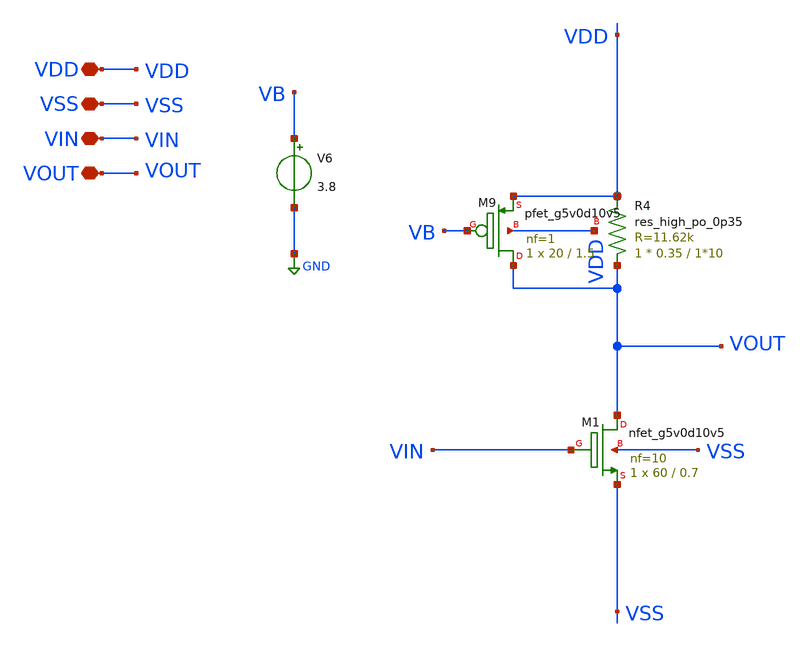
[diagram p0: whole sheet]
** sch_path: old stuff/amplifiers/single_stage_amps/stange_stages/cs_2/cs_2_stage.sch
**.subckt cs_2_stage VDD VSS VIN VOUT
*.iopin VDD
*.iopin VSS
*.iopin VIN
*.iopin VOUT
XM1 VOUT VIN VSS VSS sky130_fd_pr__nfet_g5v0d10v5 L=0.7 W=60 nf=10 ad='int((nf+1)/2) * W/nf * 0.29' as='int((nf+2)/2) * W/nf * 0.29'
+ pd='2*int((nf+1)/2) * (W/nf + 0.29)' ps='2*int((nf+2)/2) * (W/nf + 0.29)' nrd='0.29 / W' nrs='0.29 / W'
+ sa=0 sb=0 sd=0 mult=1 m=1
XR4 VOUT VDD VDD sky130_fd_pr__res_high_po_0p35 L=1*10 mult=1 m=1
XM9 VOUT VB VDD VDD sky130_fd_pr__pfet_g5v0d10v5 L=1.5 W=20 nf=1 ad='int((1 + 1)/2) * 20 / 1 * 0.29'
+ as='int((1 + 2)/2) * 20 / 1 * 0.29' pd='2*int((1 + 1)/2) * (20 / 1 + 0.29)' ps='2*int((1 + 2)/2) * (20 / 1 + 0.29)'
+ nrd='0.29 / 20 ' nrs='0.29 / 20 ' sa=0 sb=0 sd=0 mult=1 m=1
V6 VB GND 3.8
**.ends
.GLOBAL GND
.end
